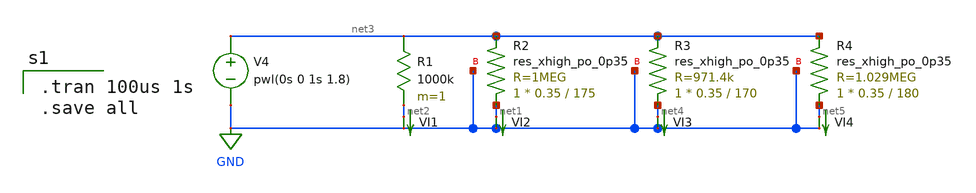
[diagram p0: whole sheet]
** sch_path: schematics/power_nfet_test.sch
**.subckt power_nfet_test
V4 net3 GND pwl(0s 0 1s 1.8)
R1 net3 net2 1000k m=1
VI1 net2 GND 0
.save i(vi1)
VI2 net1 GND 0
.save i(vi2)
XR2 net1 net3 GND sky130_fd_pr__res_xhigh_po_0p35 L=175 mult=1 m=1
XR3 net4 net3 GND sky130_fd_pr__res_xhigh_po_0p35 L=170 mult=1 m=1
VI3 net4 GND 0
.save i(vi3)
XR4 net5 net3 GND sky130_fd_pr__res_xhigh_po_0p35 L=180 mult=1 m=1
VI4 net5 GND 0
.save i(vi4)
**** begin user architecture code

.tran 100us 1s
.save all


.option wnflag=1
.lib ~/skywater/skywater-pdk/libraries/sky130_fd_pr_ngspice/latest/models/sky130.lib.spice tt

**** end user architecture code
**.ends
.GLOBAL GND
.end
